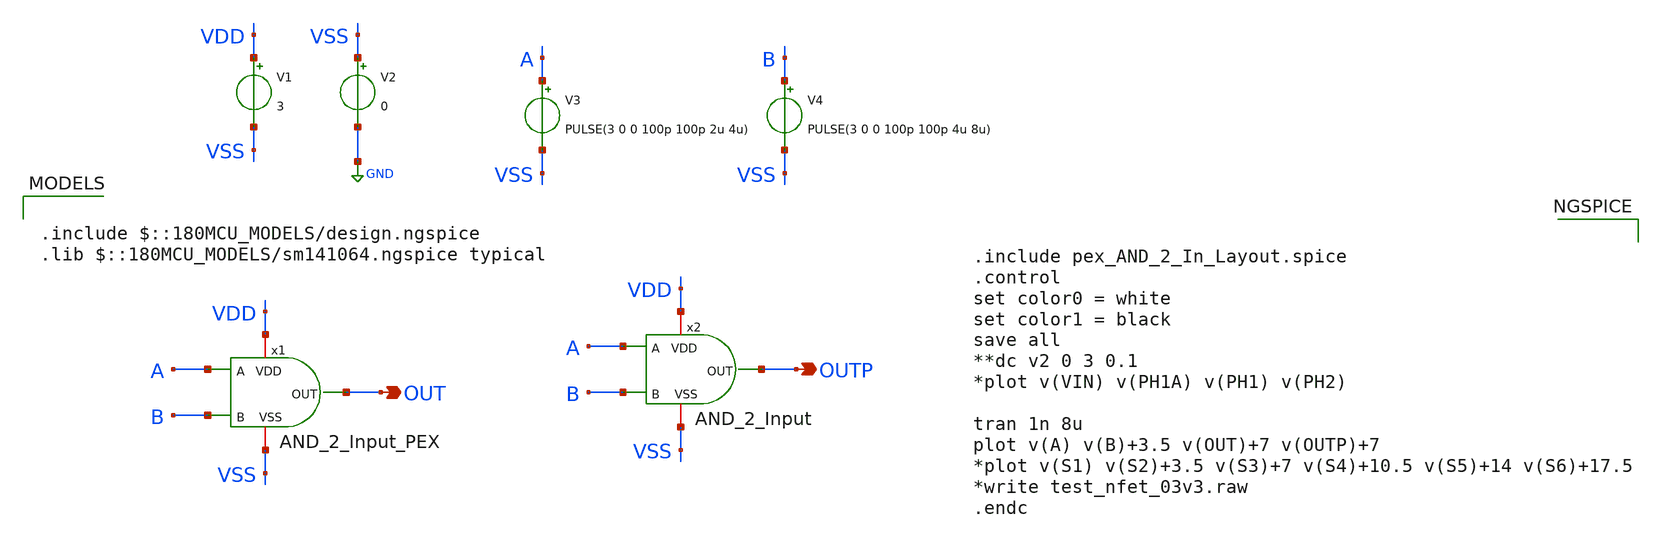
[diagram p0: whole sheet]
** sch_path: SCOP_INPUT_AND_MUX_PAKISTAN_03/Xschem/Logic_Gates/AND_2_Input_TB.sch
**.subckt AND_2_Input_TB OUT OUTP
*.opin OUT
*.opin OUTP
V1 VDD VSS 3
V2 VSS GND 0
V3 A VSS PULSE(3 0 0 100p 100p 2u 4u)
V4 B VSS PULSE(3 0 0 100p 100p 4u 8u)
x1 VDD A OUT B VSS AND_2_Input_PEX
x2 VDD A OUTP B VSS AND_2_Input
**** begin user architecture code

.include $::180MCU_MODELS/design.ngspice
.lib $::180MCU_MODELS/sm141064.ngspice typical



.include pex_AND_2_In_Layout.spice
.control
set color0 = white
set color1 = black
save all
**dc v2 0 3 0.1
*plot v(VIN) v(PH1A) v(PH1) v(PH2)

tran 1n 8u
plot v(A) v(B)+3.5 v(OUT)+7 v(OUTP)+7
*plot v(S1) v(S2)+3.5 v(S3)+7 v(S4)+10.5 v(S5)+14 v(S6)+17.5
*write test_nfet_03v3.raw
.endc


**** end user architecture code
**.ends

* expanding   symbol:  AND_2_Input.sym # of pins=5
** sym_path: SCOP_INPUT_AND_MUX_PAKISTAN_03/Xschem/Logic_Gates/AND_2_Input.sym
** sch_path: SCOP_INPUT_AND_MUX_PAKISTAN_03/Xschem/Logic_Gates/AND_2_Input.sch
.subckt AND_2_Input VDD A OUT B VSS
*.iopin VDD
*.iopin VSS
*.ipin A
*.ipin B
*.opin OUT
XM2 net2 A VDD VDD pfet_03v3 L=0.28u W=1u nf=1 ad='int((nf+1)/2) * W/nf * 0.18u' as='int((nf+2)/2) * W/nf * 0.18u'
+ pd='2*int((nf+1)/2) * (W/nf + 0.18u)' ps='2*int((nf+2)/2) * (W/nf + 0.18u)' nrd='0.18u / W' nrs='0.18u / W'
+ sa=0 sb=0 sd=0 m=1
XM3 net1 B VSS VSS nfet_03v3 L=0.28u W=1u nf=2 ad='int((nf+1)/2) * W/nf * 0.18u' as='int((nf+2)/2) * W/nf * 0.18u'
+ pd='2*int((nf+1)/2) * (W/nf + 0.18u)' ps='2*int((nf+2)/2) * (W/nf + 0.18u)' nrd='0.18u / W' nrs='0.18u / W'
+ sa=0 sb=0 sd=0 m=1
XM4 net2 A net1 VSS nfet_03v3 L=0.28u W=1u nf=2 ad='int((nf+1)/2) * W/nf * 0.18u' as='int((nf+2)/2) * W/nf * 0.18u'
+ pd='2*int((nf+1)/2) * (W/nf + 0.18u)' ps='2*int((nf+2)/2) * (W/nf + 0.18u)' nrd='0.18u / W' nrs='0.18u / W'
+ sa=0 sb=0 sd=0 m=1
XM5 net2 B VDD VDD pfet_03v3 L=0.28u W=1u nf=1 ad='int((nf+1)/2) * W/nf * 0.18u' as='int((nf+2)/2) * W/nf * 0.18u'
+ pd='2*int((nf+1)/2) * (W/nf + 0.18u)' ps='2*int((nf+2)/2) * (W/nf + 0.18u)' nrd='0.18u / W' nrs='0.18u / W'
+ sa=0 sb=0 sd=0 m=1
XM8 OUT net2 VDD VDD pfet_03v3 L=0.28u W=1u nf=1 ad='int((nf+1)/2) * W/nf * 0.18u' as='int((nf+2)/2) * W/nf * 0.18u'
+ pd='2*int((nf+1)/2) * (W/nf + 0.18u)' ps='2*int((nf+2)/2) * (W/nf + 0.18u)' nrd='0.18u / W' nrs='0.18u / W'
+ sa=0 sb=0 sd=0 m=1
XM9 OUT net2 VSS VSS nfet_03v3 L=0.28u W=0.5u nf=1 ad='int((nf+1)/2) * W/nf * 0.18u' as='int((nf+2)/2) * W/nf * 0.18u'
+ pd='2*int((nf+1)/2) * (W/nf + 0.18u)' ps='2*int((nf+2)/2) * (W/nf + 0.18u)' nrd='0.18u / W' nrs='0.18u / W'
+ sa=0 sb=0 sd=0 m=1
.ends

.GLOBAL GND
.end
